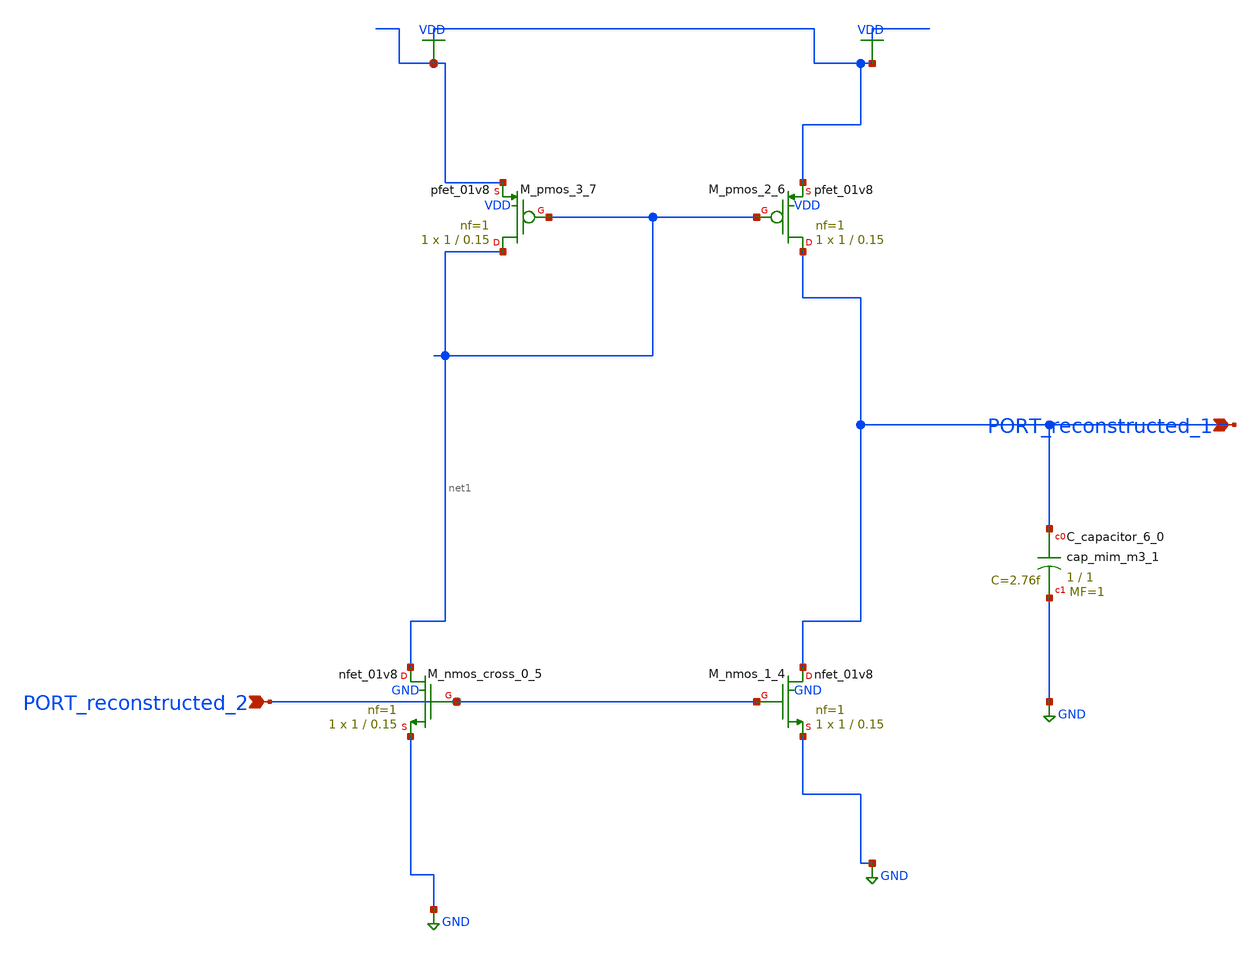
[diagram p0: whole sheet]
** sch_path: schematics/AMSNet/702.sch
**.subckt 702 PORT_reconstructed_1 PORT_reconstructed_2
*.ipin PORT_reconstructed_1
*.ipin PORT_reconstructed_2
XC_capacitor_6_0 PORT_reconstructed_1 GND sky130_fd_pr__cap_mim_m3_1 W=1 L=1 MF=1 m=1
XM_nmos_1_4 PORT_reconstructed_1 PORT_reconstructed_2 GND GND sky130_fd_pr__nfet_01v8 L=0.15 W=1 nf=1
+ ad='int((1 + 1)/2) * 1 / 1 * 0.29' as='int((1 + 2)/2) * 1 / 1 * 0.29' pd='2*int((1 + 1)/2) * (1 / 1 + 0.29)'
+ ps='2*int((1 + 2)/2) * (1 / 1 + 0.29)' nrd='0.29 / 1 ' nrs='0.29 / 1 ' sa=0 sb=0 sd=0 mult=1 m=1
XM_nmos_cross_0_5 net1 PORT_reconstructed_2 GND GND sky130_fd_pr__nfet_01v8 L=0.15 W=1 nf=1 ad='int((1 + 1)/2) * 1 / 1 * 0.29'
+ as='int((1 + 2)/2) * 1 / 1 * 0.29' pd='2*int((1 + 1)/2) * (1 / 1 + 0.29)' ps='2*int((1 + 2)/2) * (1 / 1 + 0.29)'
+ nrd='0.29 / 1 ' nrs='0.29 / 1 ' sa=0 sb=0 sd=0 mult=1 m=1
XM_pmos_2_6 PORT_reconstructed_1 net1 VDD VDD sky130_fd_pr__pfet_01v8 L=0.15 W=1 nf=1 ad='int((1 + 1)/2) * 1 / 1 * 0.29'
+ as='int((1 + 2)/2) * 1 / 1 * 0.29' pd='2*int((1 + 1)/2) * (1 / 1 + 0.29)' ps='2*int((1 + 2)/2) * (1 / 1 + 0.29)'
+ nrd='0.29 / 1 ' nrs='0.29 / 1 ' sa=0 sb=0 sd=0 mult=1 m=1
XM_pmos_3_7 net1 net1 VDD VDD sky130_fd_pr__pfet_01v8 L=0.15 W=1 nf=1 ad='int((1 + 1)/2) * 1 / 1 * 0.29'
+ as='int((1 + 2)/2) * 1 / 1 * 0.29' pd='2*int((1 + 1)/2) * (1 / 1 + 0.29)' ps='2*int((1 + 2)/2) * (1 / 1 + 0.29)'
+ nrd='0.29 / 1 ' nrs='0.29 / 1 ' sa=0 sb=0 sd=0 mult=1 m=1
**.ends
.GLOBAL GND
.GLOBAL VDD
.end
